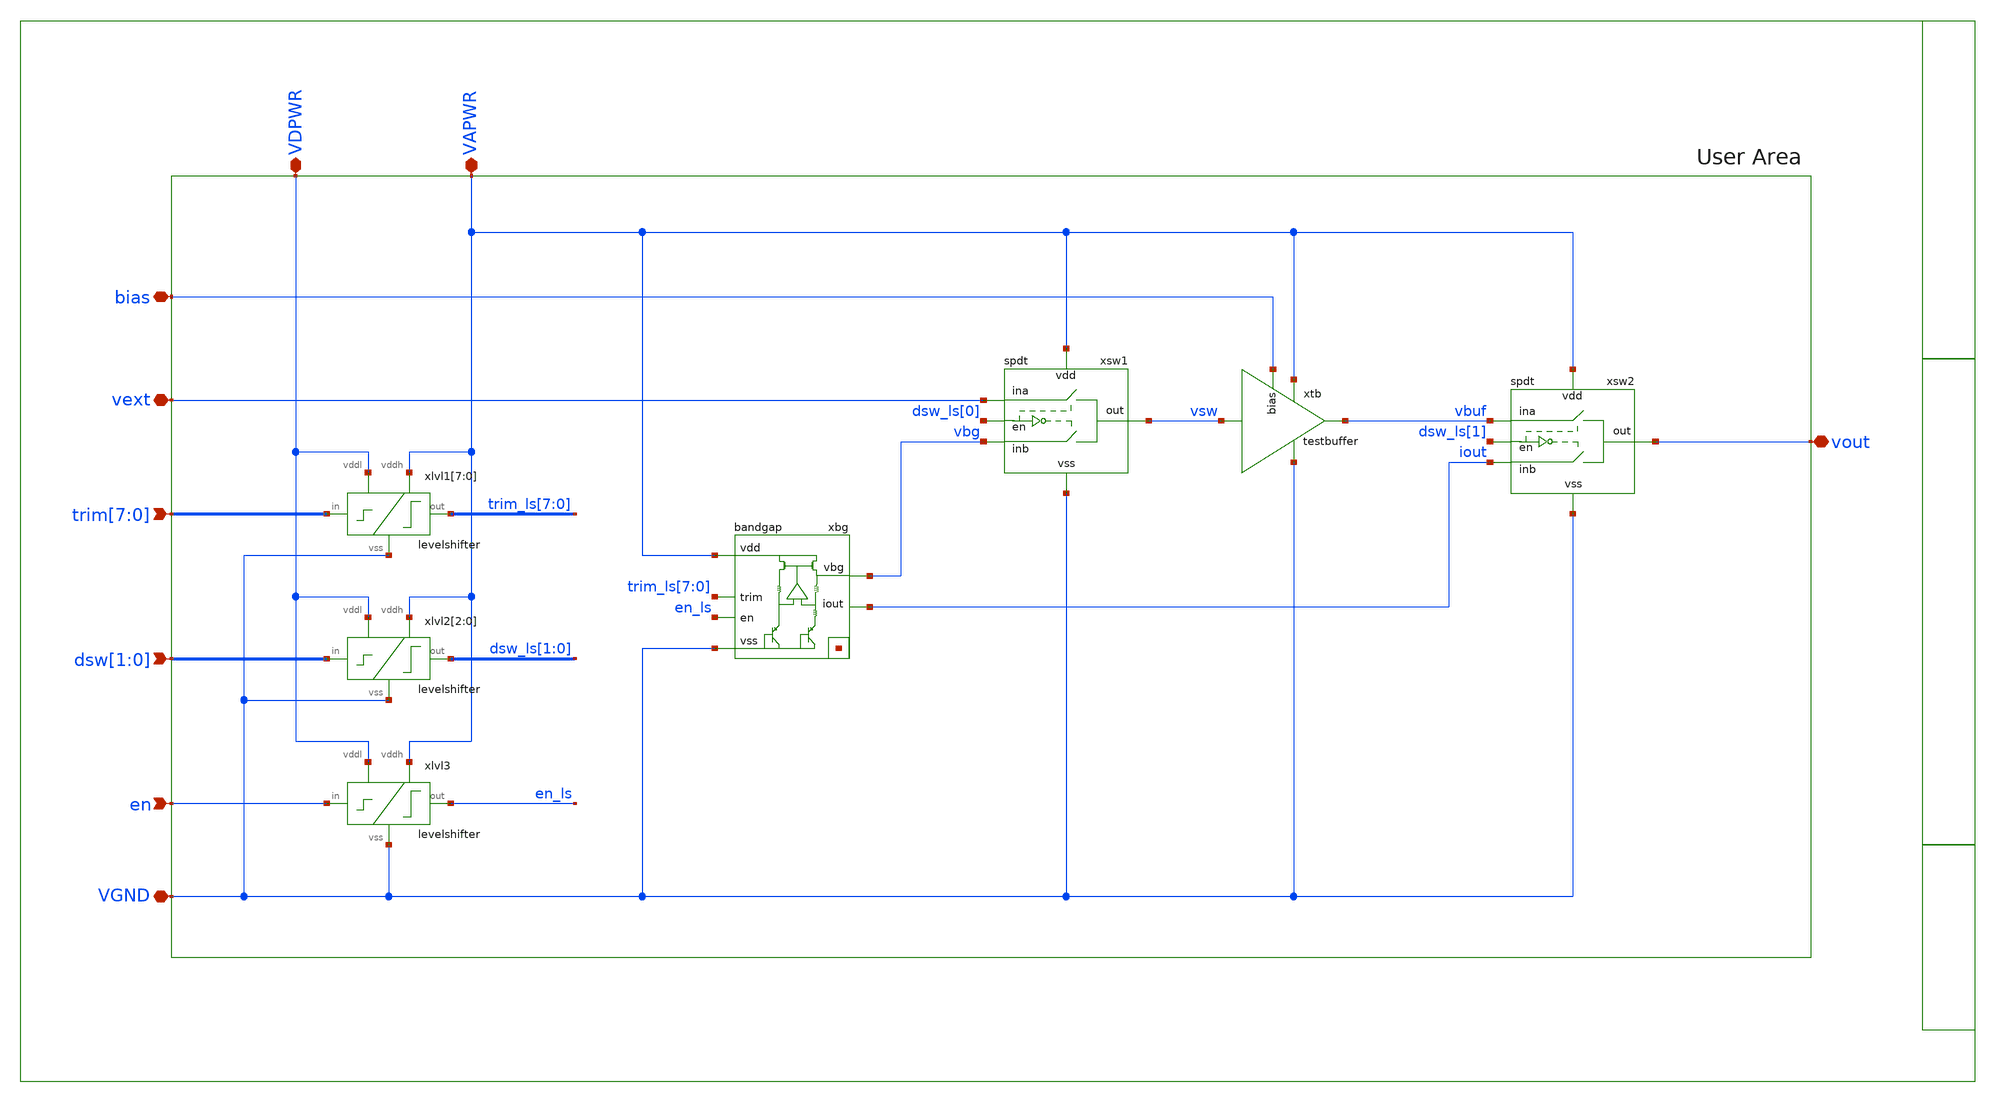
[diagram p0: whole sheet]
** sch_path: xschem/sch/top/gf180mcu_cw_ip_vref.sch
**.subckt gf180mcu_cw_ip_vref VGND VDPWR VAPWR bias
*+ trim[7],trim[6],trim[5],trim[4],trim[3],trim[2],trim[1],trim[0] dsw[1],dsw[0] vout vext en
*.iopin VGND
*.iopin VDPWR
*.iopin VAPWR
*.iopin bias
*.ipin trim[7],trim[6],trim[5],trim[4],trim[3],trim[2],trim[1],trim[0]
*.ipin dsw[1],dsw[0]
*.iopin vout
*.iopin vext
*.ipin en
xtb VAPWR vbuf vsw VGND bias testbuffer
xsw1 vsw dsw_ls[0] VAPWR vbg VGND vext spdt
xsw2 vout dsw_ls[1] VAPWR iout VGND vbuf spdt
xlvl1[7] VDPWR trim[7] trim_ls[7] VGND VAPWR levelshifter
xlvl1[6] VDPWR trim[6] trim_ls[6] VGND VAPWR levelshifter
xlvl1[5] VDPWR trim[5] trim_ls[5] VGND VAPWR levelshifter
xlvl1[4] VDPWR trim[4] trim_ls[4] VGND VAPWR levelshifter
xlvl1[3] VDPWR trim[3] trim_ls[3] VGND VAPWR levelshifter
xlvl1[2] VDPWR trim[2] trim_ls[2] VGND VAPWR levelshifter
xlvl1[1] VDPWR trim[1] trim_ls[1] VGND VAPWR levelshifter
xlvl1[0] VDPWR trim[0] trim_ls[0] VGND VAPWR levelshifter
xlvl2[2] VDPWR dsw[1] dsw_ls[1] VGND VAPWR levelshifter
xlvl2[1] VDPWR dsw[0] dsw_ls[0] VGND VAPWR levelshifter
xlvl2[0] VDPWR dsw[1] dsw_ls[1] VGND VAPWR levelshifter
xbg VAPWR vbg VGND net1[7] net1[6] net1[5] net1[4] net1[3] net1[2] net1[1] net1[0] trim_ls[7]
+ trim_ls[6] trim_ls[5] trim_ls[4] trim_ls[3] trim_ls[2] trim_ls[1] trim_ls[0] iout en_ls bandgap
xlvl3 VDPWR en en_ls VGND VAPWR levelshifter
**.ends
.end
